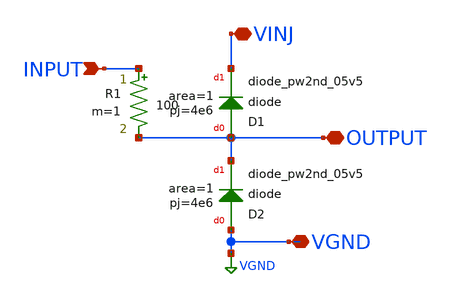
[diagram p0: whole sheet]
** sch_path: libs.ref/sky130_hilas_sc/xschem/sky130_hilas_VinjDiodeProtect01.sch
**.subckt sky130_hilas_VinjDiodeProtect01 INPUT VINJ OUTPUT VGND
*.ipin INPUT
*.iopin VINJ
*.iopin OUTPUT
*.iopin VGND
XD1 OUTPUT VINJ sky130_fd_pr__diode_pw2nd_05v5 area=1 pj=4e6
XD2 VGND OUTPUT sky130_fd_pr__diode_pw2nd_05v5 area=1 pj=4e6
R1 INPUT OUTPUT 100 m=1
**.ends
.GLOBAL VGND
.end
